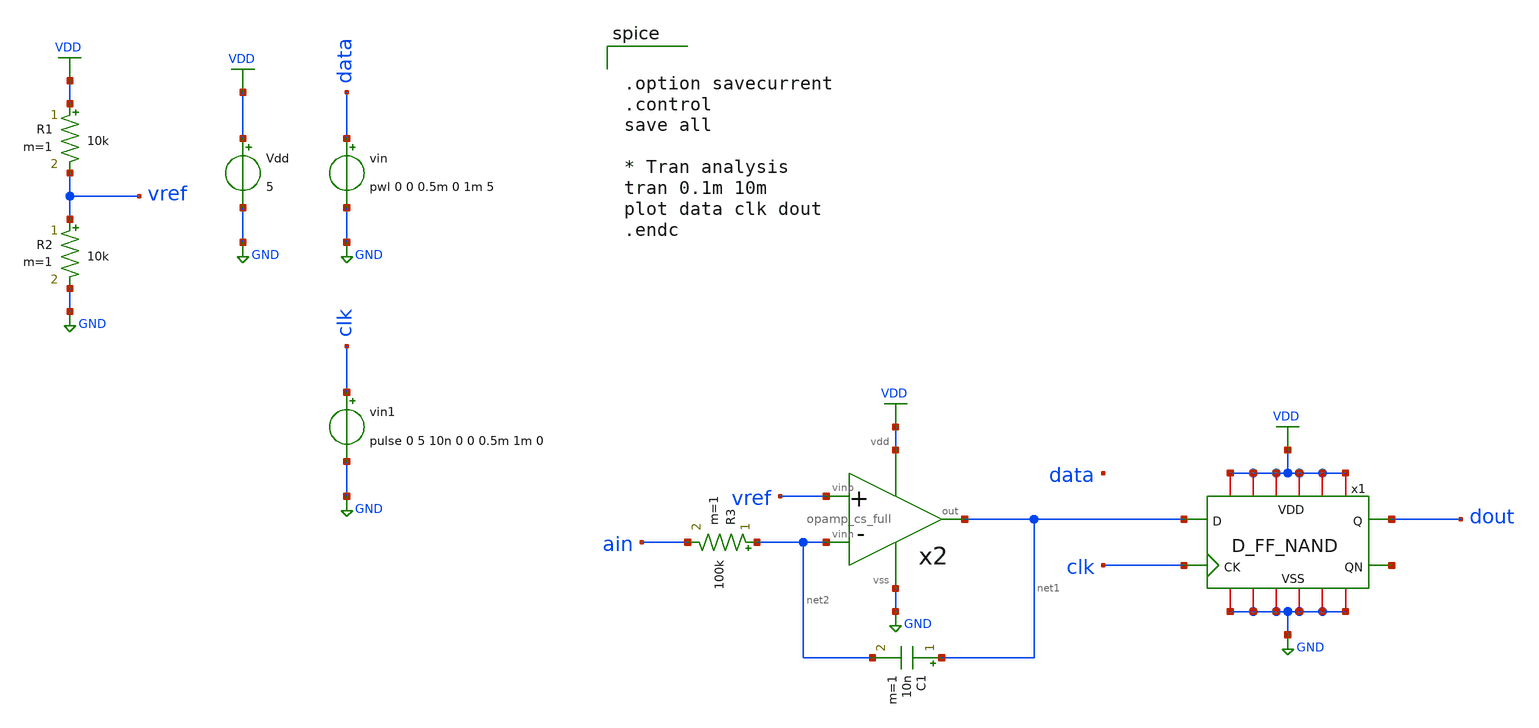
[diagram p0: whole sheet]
** sch_path: member_project/YutakaKOTANI/tb_delta_sigma_modulator.sch
**.subckt tb_delta_sigma_modulator
Vdd VDD GND 5
vin data GND pwl 0 0 0.5m 0 1m 5
x1 VDD GND dout clk net3 net1 D_FF_NAND
vin1 clk GND pulse 0 5 10n 0 0 0.5m 1m 0
x2 vref net2 net1 VDD GND opamp_cs_full
R1 VDD vref 10k m=1
R2 vref GND 10k m=1
C1 net1 net2 10n m=1
R3 net2 ain 100k m=1
**** begin user architecture code
 .include $::LIB/mos.lib
.include $::LIB/passive.lib
.include $::LIB/diode.lib


.option savecurrent
.control
save all

* Tran analysis
tran 0.1m 10m
plot data clk dout
.endc


**** end user architecture code
**.ends
.GLOBAL VDD
.GLOBAL GND
.end
